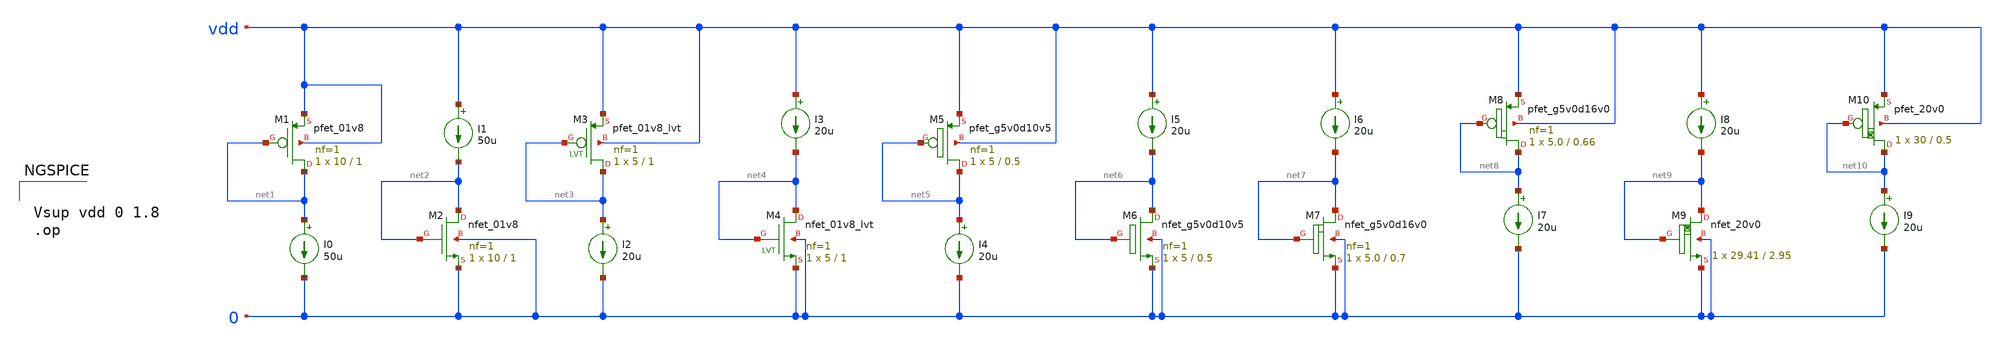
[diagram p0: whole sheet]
** sch_path: testing/test_mos.sch
**.subckt test_mos
XM1 net1 net1 vdd vdd sky130_fd_pr__pfet_01v8 L=1 W=10 nf=1 ad='int((nf+1)/2) * W/nf * 0.29' as='int((nf+2)/2) * W/nf * 0.29'
+ pd='2*int((nf+1)/2) * (W/nf + 0.29)' ps='2*int((nf+2)/2) * (W/nf + 0.29)' nrd='0.29 / W' nrs='0.29 / W'
+ sa=0 sb=0 sd=0 mult=1 m=1
I0 net1 0 50u
XM2 net2 net2 0 0 sky130_fd_pr__nfet_01v8 L=1 W=10 nf=1 ad='int((nf+1)/2) * W/nf * 0.29' as='int((nf+2)/2) * W/nf * 0.29'
+ pd='2*int((nf+1)/2) * (W/nf + 0.29)' ps='2*int((nf+2)/2) * (W/nf + 0.29)' nrd='0.29 / W' nrs='0.29 / W'
+ sa=0 sb=0 sd=0 mult=1 m=1
I1 vdd net2 50u
XM3 net3 net3 vdd vdd sky130_fd_pr__pfet_01v8_lvt L=1 W=5 nf=1 ad='int((nf+1)/2) * W/nf * 0.29' as='int((nf+2)/2) * W/nf * 0.29'
+ pd='2*int((nf+1)/2) * (W/nf + 0.29)' ps='2*int((nf+2)/2) * (W/nf + 0.29)' nrd='0.29 / W' nrs='0.29 / W'
+ sa=0 sb=0 sd=0 mult=1 m=1
I2 net3 0 20u
I3 vdd net4 20u
I4 net5 0 20u
I5 vdd net6 20u
XM4 net4 net4 0 0 sky130_fd_pr__nfet_01v8_lvt L=1 W=5 nf=1 ad='int((nf+1)/2) * W/nf * 0.29' as='int((nf+2)/2) * W/nf * 0.29'
+ pd='2*int((nf+1)/2) * (W/nf + 0.29)' ps='2*int((nf+2)/2) * (W/nf + 0.29)' nrd='0.29 / W' nrs='0.29 / W'
+ sa=0 sb=0 sd=0 mult=1 m=1
XM5 net5 net5 vdd vdd sky130_fd_pr__pfet_g5v0d10v5 L=0.5 W=5 nf=1 ad='int((nf+1)/2) * W/nf * 0.29' as='int((nf+2)/2) * W/nf * 0.29'
+ pd='2*int((nf+1)/2) * (W/nf + 0.29)' ps='2*int((nf+2)/2) * (W/nf + 0.29)' nrd='0.29 / W' nrs='0.29 / W'
+ sa=0 sb=0 sd=0 mult=1 m=1
XM6 net6 net6 0 0 sky130_fd_pr__nfet_g5v0d10v5 L=0.5 W=5 nf=1 ad='int((nf+1)/2) * W/nf * 0.29' as='int((nf+2)/2) * W/nf * 0.29'
+ pd='2*int((nf+1)/2) * (W/nf + 0.29)' ps='2*int((nf+2)/2) * (W/nf + 0.29)' nrd='0.29 / W' nrs='0.29 / W'
+ sa=0 sb=0 sd=0 mult=1 m=1
I6 vdd net7 20u
XM7 net7 net7 0 0 sky130_fd_pr__nfet_g5v0d16v0 L=0.7 W=5.0 nf=1 ad='int((nf+1)/2) * W/nf * 0.29' as='int((nf+2)/2) * W/nf * 0.29'
+ pd='2*int((nf+1)/2) * (W/nf + 0.29)' ps='2*int((nf+2)/2) * (W/nf + 0.29)' nrd='0.29 / W' nrs='0.29 / W'
+ sa=0 sb=0 sd=0 mult=1 m=1
XM8 net8 net8 vdd vdd sky130_fd_pr__pfet_g5v0d16v0 L=0.66 W=5.0 nf=1 ad='int((nf+1)/2) * W/nf * 0.29'
+ as='int((nf+2)/2) * W/nf * 0.29' pd='2*int((nf+1)/2) * (W/nf + 0.29)' ps='2*int((nf+2)/2) * (W/nf + 0.29)'
+ nrd='0.29 / W' nrs='0.29 / W' sa=0 sb=0 sd=0 mult=1 m=1
I7 net8 0 20u
I8 vdd net9 20u
I9 net10 0 20u
XM9 net9 net9 0 0 sky130_fd_pr__nfet_20v0 L=2.95 W=29.41 m=1
XM10 net10 net10 vdd vdd sky130_fd_pr__pfet_20v0 L=0.5 W=30 m=1
**** begin user architecture code


Vsup vdd 0 1.8
.op




.param mc_mm_switch=0
.param mc_pr_switch=0
.include ~/mabrains/Analog_blocks/models/sky130A/libs.ref/sky130_fd_pr/spice/sky130_fd_pr__nfet_01v8__tt.corner.spice
.include ~/mabrains/Analog_blocks/models/sky130A/libs.ref/sky130_fd_pr/spice/sky130_fd_pr__nfet_01v8_lvt__tt.corner.spice
.include ~/mabrains/Analog_blocks/models/sky130A/libs.ref/sky130_fd_pr/spice/sky130_fd_pr__pfet_01v8__tt.corner.spice
.include ~/mabrains/Analog_blocks/models/sky130A/libs.ref/sky130_fd_pr/spice/sky130_fd_pr__nfet_03v3_nvt__tt.corner.spice
.include ~/mabrains/Analog_blocks/models/sky130A/libs.ref/sky130_fd_pr/spice/sky130_fd_pr__nfet_05v0_nvt__tt.corner.spice
.include ~/mabrains/Analog_blocks/models/sky130A/libs.ref/sky130_fd_pr/spice/sky130_fd_pr__esd_nfet_01v8__tt.corner.spice
.include ~/mabrains/Analog_blocks/models/sky130A/libs.ref/sky130_fd_pr/spice/sky130_fd_pr__pfet_01v8_lvt__tt.corner.spice
.include ~/mabrains/Analog_blocks/models/sky130A/libs.ref/sky130_fd_pr/spice/sky130_fd_pr__pfet_01v8_hvt__tt.corner.spice
.include ~/mabrains/Analog_blocks/models/sky130A/libs.ref/sky130_fd_pr/spice/sky130_fd_pr__esd_pfet_g5v0d10v5__tt.corner.spice
.include ~/mabrains/Analog_blocks/models/sky130A/libs.ref/sky130_fd_pr/spice/sky130_fd_pr__pfet_g5v0d10v5__tt.corner.spice
.include ~/mabrains/Analog_blocks/models/sky130A/libs.ref/sky130_fd_pr/spice/sky130_fd_pr__pfet_g5v0d16v0__tt.corner.spice
.include ~/mabrains/Analog_blocks/models/sky130A/libs.ref/sky130_fd_pr/spice/sky130_fd_pr__nfet_g5v0d10v5__tt.corner.spice
.include ~/mabrains/Analog_blocks/models/sky130A/libs.ref/sky130_fd_pr/spice/sky130_fd_pr__nfet_g5v0d16v0__tt_discrete.corner.spice
.include ~/mabrains/Analog_blocks/models/sky130A/libs.ref/sky130_fd_pr/spice/sky130_fd_pr__esd_nfet_g5v0d10v5__tt.corner.spice
.include ~/mabrains/Analog_blocks/models/sky130A/libs.ref/sky130_fd_pr/spice/sky130_fd_pr__pfet_20v0__tt_discrete.corner.spice
.include ~/mabrains/Analog_blocks/models/sky130A/libs.ref/sky130_fd_pr/spice/sky130_fd_pr__nfet_20v0__tt_discrete.corner.spice
.include ~/mabrains/Analog_blocks/models/sky130A/libs.tech/ngspice/corners/tt/nonfet.spice
* Mismatch parameters
.include ~/mabrains/Analog_blocks/models/sky130A/libs.ref/sky130_fd_pr/spice/sky130_fd_pr__nfet_01v8__mismatch.corner.spice
.include ~/mabrains/Analog_blocks/models/sky130A/libs.ref/sky130_fd_pr/spice/sky130_fd_pr__pfet_01v8__mismatch.corner.spice
.include ~/mabrains/Analog_blocks/models/sky130A/libs.ref/sky130_fd_pr/spice/sky130_fd_pr__nfet_01v8_lvt__mismatch.corner.spice
.include ~/mabrains/Analog_blocks/models/sky130A/libs.ref/sky130_fd_pr/spice/sky130_fd_pr__pfet_01v8_lvt__mismatch.corner.spice
.include ~/mabrains/Analog_blocks/models/sky130A/libs.ref/sky130_fd_pr/spice/sky130_fd_pr__pfet_01v8_hvt__mismatch.corner.spice
.include ~/mabrains/Analog_blocks/models/sky130A/libs.ref/sky130_fd_pr/spice/sky130_fd_pr__nfet_g5v0d10v5__mismatch.corner.spice
.include ~/mabrains/Analog_blocks/models/sky130A/libs.ref/sky130_fd_pr/spice/sky130_fd_pr__pfet_g5v0d10v5__mismatch.corner.spice
.include ~/mabrains/Analog_blocks/models/sky130A/libs.ref/sky130_fd_pr/spice/sky130_fd_pr__nfet_05v0_nvt__mismatch.corner.spice
.include ~/mabrains/Analog_blocks/models/sky130A/libs.ref/sky130_fd_pr/spice/sky130_fd_pr__nfet_03v3_nvt__mismatch.corner.spice
* Resistor/Capacitor
.include ~/mabrains/Analog_blocks/models/sky130A/libs.tech/ngspice/r+c/res_typical__cap_typical.spice
.include ~/mabrains/Analog_blocks/models/sky130A/libs.tech/ngspice/r+c/res_typical__cap_typical__lin.spice
* Special cells
.include ~/mabrains/Analog_blocks/models/sky130A/libs.tech/ngspice/corners/tt/specialized_cells.spice
* All models
.include ~/mabrains/Analog_blocks/models/sky130A/libs.tech/ngspice/all.spice
* Corner
.include ~/mabrains/Analog_blocks/models/sky130A/libs.tech/ngspice/corners/tt/rf.spice



**** end user architecture code
**.ends
.end
